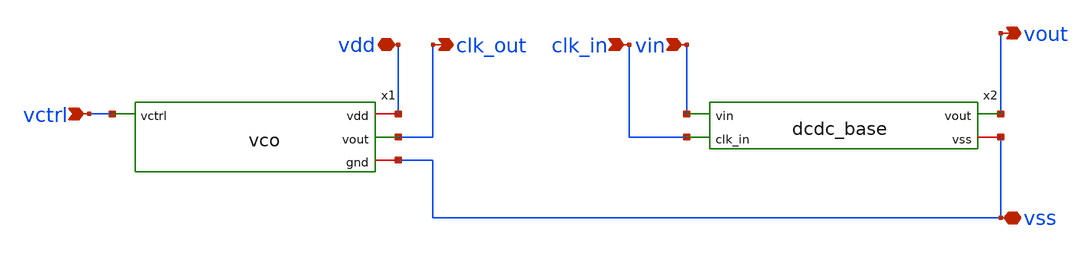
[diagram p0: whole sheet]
** sch_path: member_project/DCDC_DOWN/xschem/dcdc_down.sch
**.subckt dcdc_down vin vout vss vdd vctrl clk_in clk_out
*.ipin vin
*.opin vout
*.iopin vss
*.iopin vdd
*.ipin vctrl
*.ipin clk_in
*.opin clk_out
x1 vdd clk_out vctrl vss vco
x2 vin vout clk_in vss dcdc_base
**.ends

* expanding   symbol:  vco.sym # of pins=4
** sym_path: member_project/DCDC_DOWN/xschem/original_VCO/vco.sym
** sch_path: member_project/DCDC_DOWN/xschem/original_VCO/vco.sch
.subckt vco vdd vout vctrl gnd
*.iopin vdd
*.opin vout
*.iopin gnd
*.ipin vctrl
M4 vdd net1 net1 vdd pchor1ex L=20u W=12u m=1
M6 net2 vctrl gnd gnd nchor1ex L=20u W=4u m=1
x2 vdd net1 net3 net8 vctrl gnd inverter
x3 vdd net1 net4 net3 vctrl gnd inverter
x4 vdd net1 net6 net4 vctrl gnd inverter
x5 vdd net1 net5 net6 vctrl gnd inverter
x1 vdd vout net6 gnd buffer
x9 vdd net1 net7 net5 vctrl gnd inverter
x6 vdd net1 net9 net7 vctrl gnd inverter
x7 vdd net1 net8 net9 vctrl gnd inverter
M1 net1 net1 net2 gnd nchor1ex L=20u W=4u m=1
.ends


* expanding   symbol:  dcdc_base.sym # of pins=4
** sym_path: member_project/DCDC_DOWN/xschem/dcdc_base.sym
** sch_path: member_project/DCDC_DOWN/xschem/dcdc_base.sch
.subckt dcdc_base vin vout clk_in vss
*.ipin clk_in
*.ipin vin
*.iopin vss
*.opin vout
M1 vin clk_in vout vss nchor1ex L=1.0u W=40.0u m=1
M2 vin vss vout vss nchor1ex L=3.0u W=40.0u m=1
M3 vout vss vss vss nchor1ex L=3.0u W=40.0u m=1
.ends


* expanding   symbol:  inverter.sym # of pins=6
** sym_path: member_project/DCDC_DOWN/xschem/original_VCO/inverter.sym
** sch_path: member_project/DCDC_DOWN/xschem/original_VCO/inverter.sch
.subckt inverter vdd vvctrl vout vin vctrl gnd
*.ipin vin
*.opin vout
*.iopin vdd
*.iopin gnd
*.ipin vctrl
*.ipin vvctrl
M1 vout vin net1 vdd pchor1ex L=1u W=3u m=1
M2 vout vin net2 gnd nchor1ex L=1u W=1u m=1
M3 net2 vctrl gnd gnd nchor1ex L=20u W=2u m=1
M4 net1 vvctrl vdd vdd pchor1ex L=20u W=6u m=1
C2 vout gnd poly_cap W=20 L=20
.ends


* expanding   symbol:  buffer.sym # of pins=4
** sym_path: member_project/DCDC_DOWN/xschem/original_VCO/buffer.sym
** sch_path: member_project/DCDC_DOWN/xschem/original_VCO/buffer.sch
.subckt buffer vdd vout vin gnd
*.iopin vdd
*.ipin vin
*.opin vout
*.iopin gnd
M1 net1 vin gnd gnd nchor1ex L=1u W=1u m=1
M2 net1 vin vdd vdd pchor1ex L=1u W=3u m=1
M3 vout net1 gnd gnd nchor1ex L=1u W=1u m=1
M4 vout net1 vdd vdd pchor1ex L=1u W=3u m=1
.ends

.end
